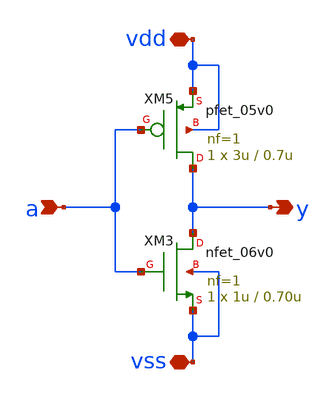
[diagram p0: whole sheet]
** sch_path: member_project/ice458/dynamic_comparator/xschem/inv_5v.sch
**.subckt inv_5v vdd vss a y
*.iopin vdd
*.iopin vss
*.ipin a
*.opin y
XM3 y a vss vss nfet_06v0 L=0.70u W=1u nf=1 ad='int((nf+1)/2) * W/nf * 0.18u' as='int((nf+2)/2) * W/nf * 0.18u'
+ pd='2*int((nf+1)/2) * (W/nf + 0.18u)' ps='2*int((nf+2)/2) * (W/nf + 0.18u)' nrd='0.18u / W' nrs='0.18u / W'
+ sa=0 sb=0 sd=0 m=1
XM5 y a vdd vdd pfet_05v0 L=0.7u W=3u nf=1 ad='int((nf+1)/2) * W/nf * 0.18u' as='int((nf+2)/2) * W/nf * 0.18u'
+ pd='2*int((nf+1)/2) * (W/nf + 0.18u)' ps='2*int((nf+2)/2) * (W/nf + 0.18u)' nrd='0.18u / W' nrs='0.18u / W'
+ sa=0 sb=0 sd=0 m=1
**.ends
.end
